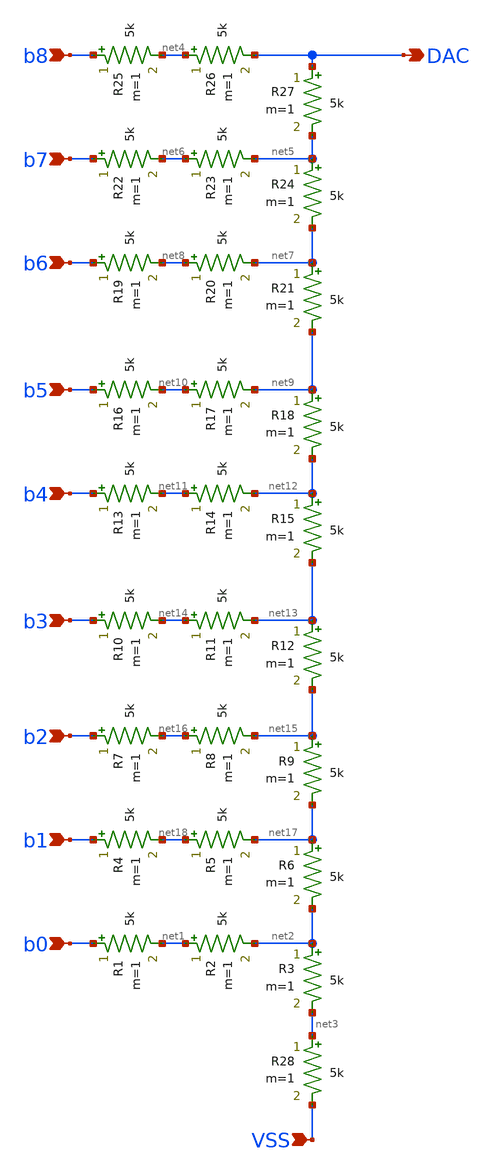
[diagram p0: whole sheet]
** sch_path: hgu/xschem/hgu_DAC.sch
**.subckt hgu_DAC b0 b1 b2 b3 b4 b5 b6 b7 b8 VSS DAC
*.ipin b0
*.ipin b1
*.ipin b2
*.ipin b3
*.ipin b4
*.ipin b5
*.ipin b6
*.ipin b7
*.ipin b8
*.ipin VSS
*.opin DAC
R1 b0 net1 5k m=1
R2 net1 net2 5k m=1
R3 net2 net3 5k m=1
R4 b1 net18 5k m=1
R5 net18 net17 5k m=1
R6 net17 net2 5k m=1
R7 b2 net16 5k m=1
R8 net16 net15 5k m=1
R9 net15 net17 5k m=1
R10 b3 net14 5k m=1
R11 net14 net13 5k m=1
R12 net13 net15 5k m=1
R13 b4 net11 5k m=1
R14 net11 net12 5k m=1
R15 net12 net13 5k m=1
R16 b5 net10 5k m=1
R17 net10 net9 5k m=1
R18 net9 net12 5k m=1
R19 b6 net8 5k m=1
R20 net8 net7 5k m=1
R21 net7 net9 5k m=1
R22 b7 net6 5k m=1
R23 net6 net5 5k m=1
R24 net5 net7 5k m=1
R25 b8 net4 5k m=1
R26 net4 DAC 5k m=1
R27 DAC net5 5k m=1
R28 net3 VSS 5k m=1
**.ends
.end
